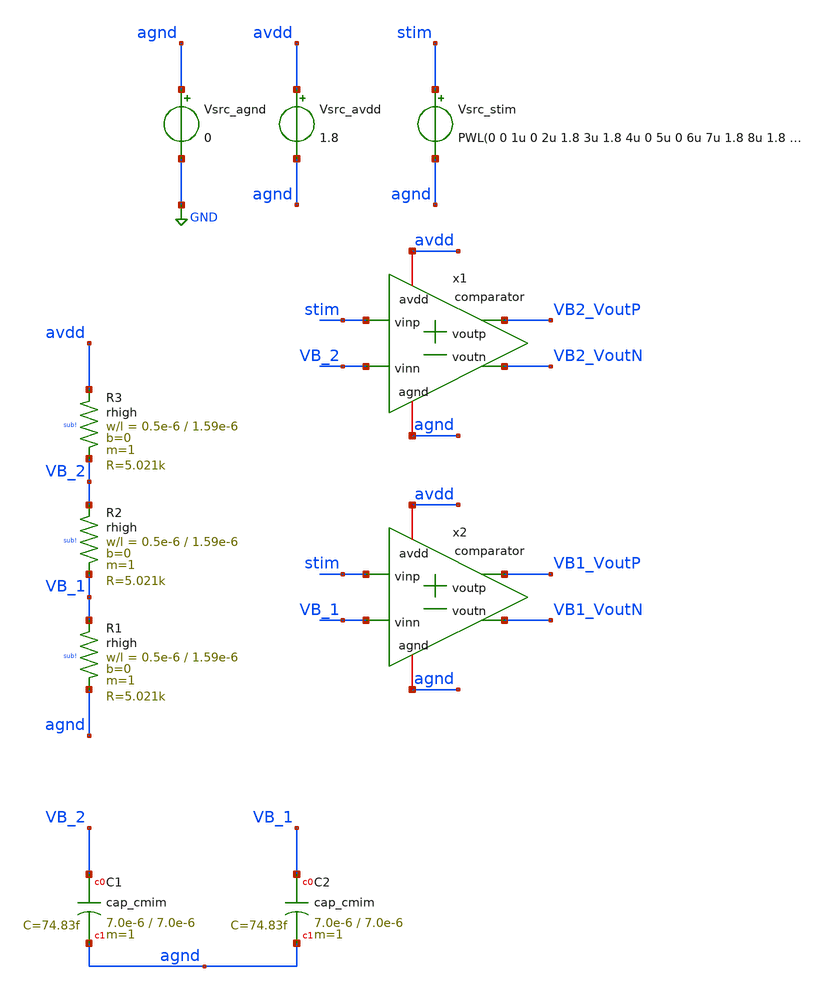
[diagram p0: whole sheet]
** sch_path: xschem/TB_comparator.sch
**.subckt TB_comparator
x1 avdd VB2_VoutP VB2_VoutN VB_2 stim agnd comparator
Vsrc_agnd agnd GND 0
Vsrc_avdd avdd agnd 1.8
x2 avdd VB1_VoutP VB1_VoutN VB_1 stim agnd comparator
XR3 avdd VB_2 sub! rhigh w=0.5e-6 l=1.59e-6 m=1 b=0 mm_ok=1
Vsrc_stim stim agnd PWL(0 0 1u 0 2u 1.8 3u 1.8 4u 0 5u 0 6u 7u 1.8 8u 1.8 9u 0 10u 0)
XR1 VB_1 agnd sub! rhigh w=0.5e-6 l=1.59e-6 m=1 b=0 mm_ok=1
XR2 VB_2 VB_1 sub! rhigh w=0.5e-6 l=1.59e-6 m=1 b=0 mm_ok=1
XC1 VB_2 agnd cap_cmim w=7.0e-6 l=7.0e-6 m=1 mm_ok=1
XC2 VB_1 agnd cap_cmim w=7.0e-6 l=7.0e-6 m=1 mm_ok=1
**** begin user architecture code


.lib /foss/designs/IHP-Open-PDK/ihp-sg13g2/libs.tech/ngspice/models/cornerHBT.lib hbt_typ
*.lib /foss/designs/IHP-Open-PDK/ihp-sg13g2/libs.tech/ngspice/models/cornerHBT.lib hbt_typ_stat
.lib /foss/designs/IHP-Open-PDK/ihp-sg13g2/libs.tech/ngspice/models/cornerRES.lib res_typ
*.lib /foss/designs/IHP-Open-PDK/ihp-sg13g2/libs.tech/ngspice/models/cornerRES.lib res_typ_stat
.lib /foss/designs/IHP-Open-PDK/ihp-sg13g2/libs.tech/ngspice/models/cornerMOSlv.lib mos_tt

.include /foss/designs/IHP-Open-PDK/ihp-sg13g2/libs.ref/sg13g2_stdcell/spice/sg13g2_stdcell.spice

*.lib /foss/designs/IHP-Open-PDK/ihp-sg13g2/libs.tech/ngspice/models/resistors_stat.lib
*.lib /foss/designs/IHP-Open-PDK/ihp-sg13g2/libs.tech/ngspice/models/resistors_mod.lib

* this option enables mos model bin
* selection based on W/NF instead of W
.option wnflag=1

.option savecurrents

.control
save all
op

* Print newline
echo

* Stimulus voltage
*Vstim stim 0 DC=0V
*.param Vstim = PWL(0 0 1u 1.8 2u 0 3u 1.8 4u 0)

* Sweep frequency and time
write TB_comparator.raw
set appendwrite

* Analyses
ac dec 100 1 1e11
tran 10n 10u
dc
remzerovec

* Inputs
let vin_stim = v(stim)

* Outputs
let vout_P2 = v(VB2_VoutP)
let vout_N2 = v(VB2_VoutN)
let vout_P1 = v(VB1_VoutP)
let vout_N1 = v(VB1_VoutN)

* Plot outputs
*plot v(VB_2)
*plot v(VB_1)
*plot v(stim)

write TB_comparator.raw
set appendwrite

.endc


**** end user architecture code
**.ends

* expanding   symbol:  comparator.sym # of pins=6
** sym_path: xschem/comparator.sym
** sch_path: xschem/comparator.sch
.subckt comparator avdd voutp voutn vinn vinp agnd
*.iopin avdd
*.ipin vinp
*.opin voutp
*.iopin agnd
*.ipin vinn
*.opin voutn
XQ1 voutp vinn net1 agnd npn13G2 Nx=1 mm_ok=1
XR1 avdd voutp sub! rppd w=0.5e-6 l=7.5e-6 m=1 b=0 mm_ok=1
XR2 net1 agnd sub! rppd w=0.5e-6 l=0.5e-6 m=1 b=0 mm_ok=1
XR3 avdd voutn sub! rppd w=0.5e-6 l=7.5e-6 m=1 b=0 mm_ok=1
XQ2 voutn vinp net1 agnd npn13G2 Nx=1 mm_ok=1
.ends

.GLOBAL GND
.end
